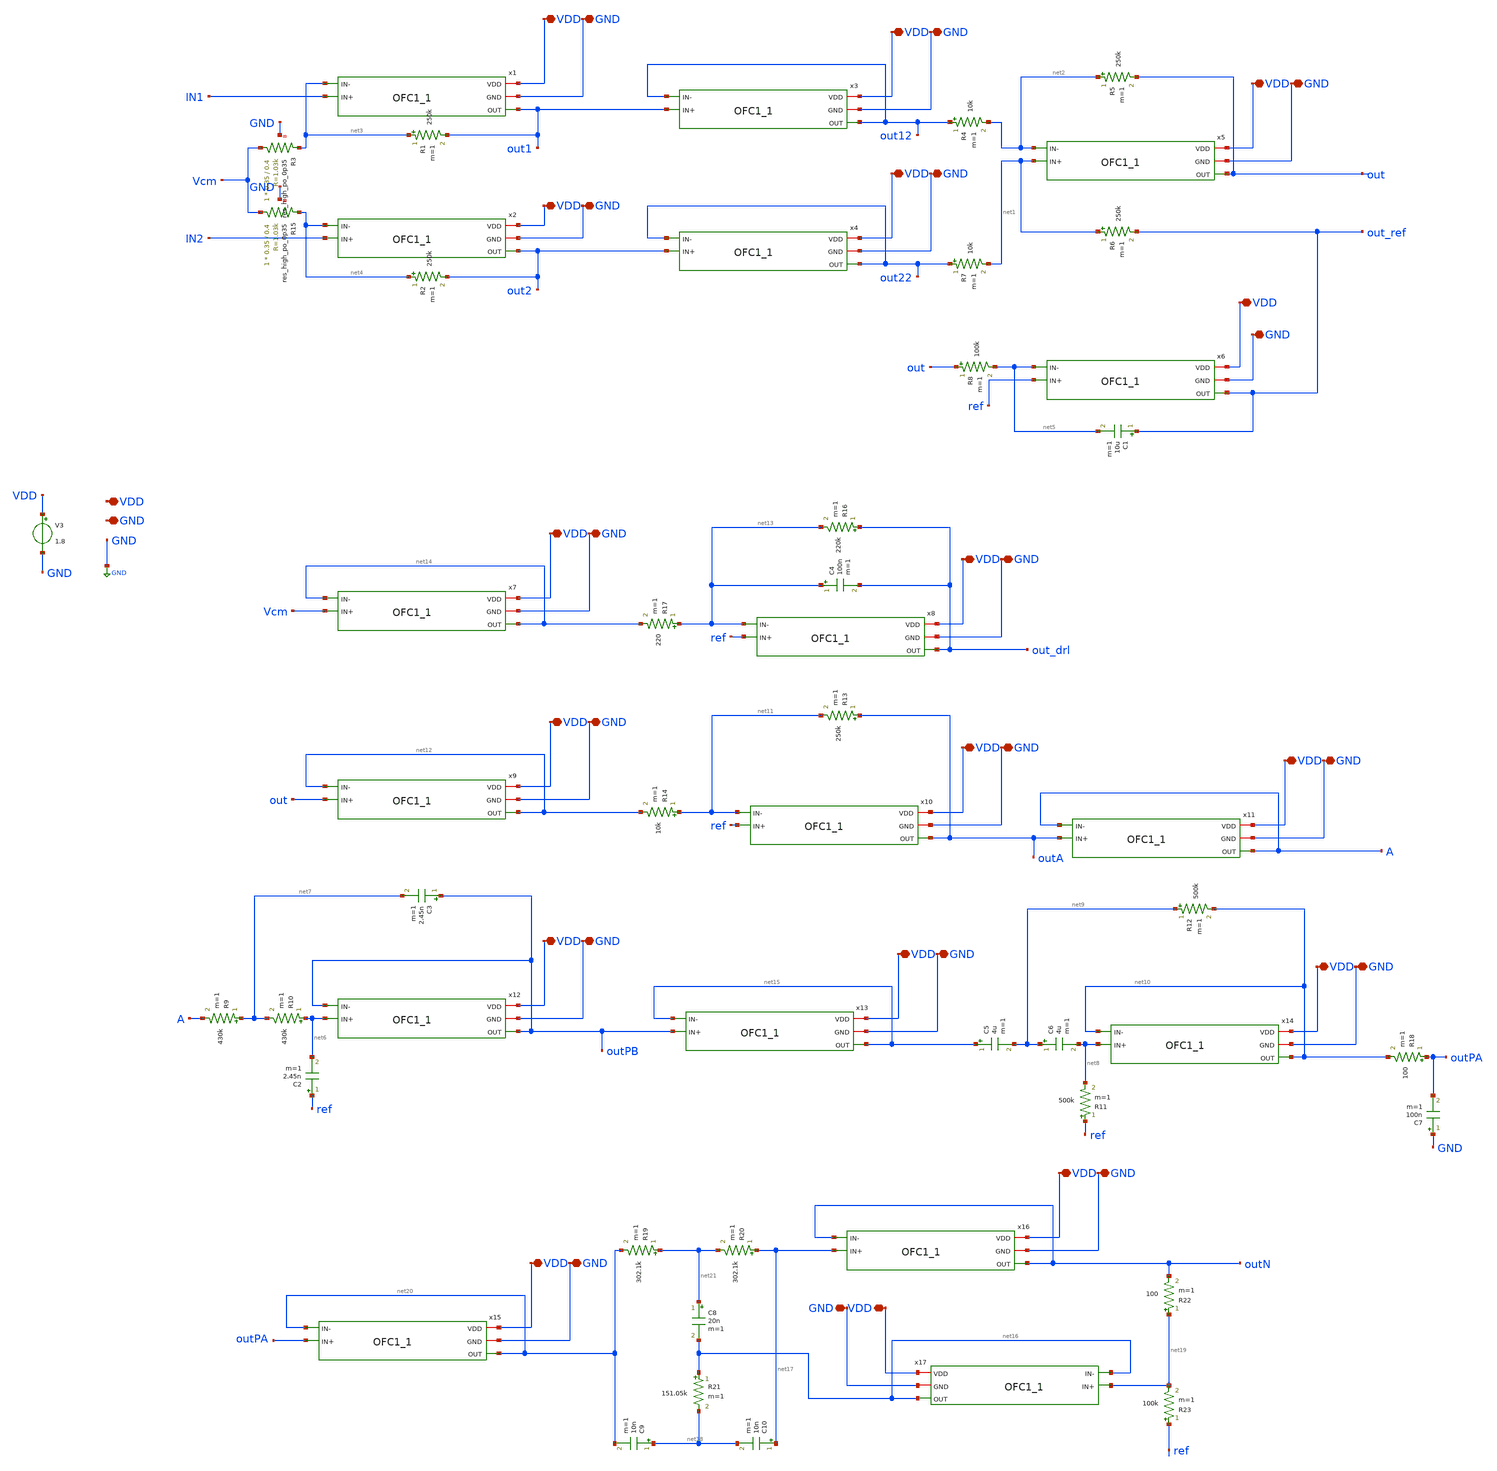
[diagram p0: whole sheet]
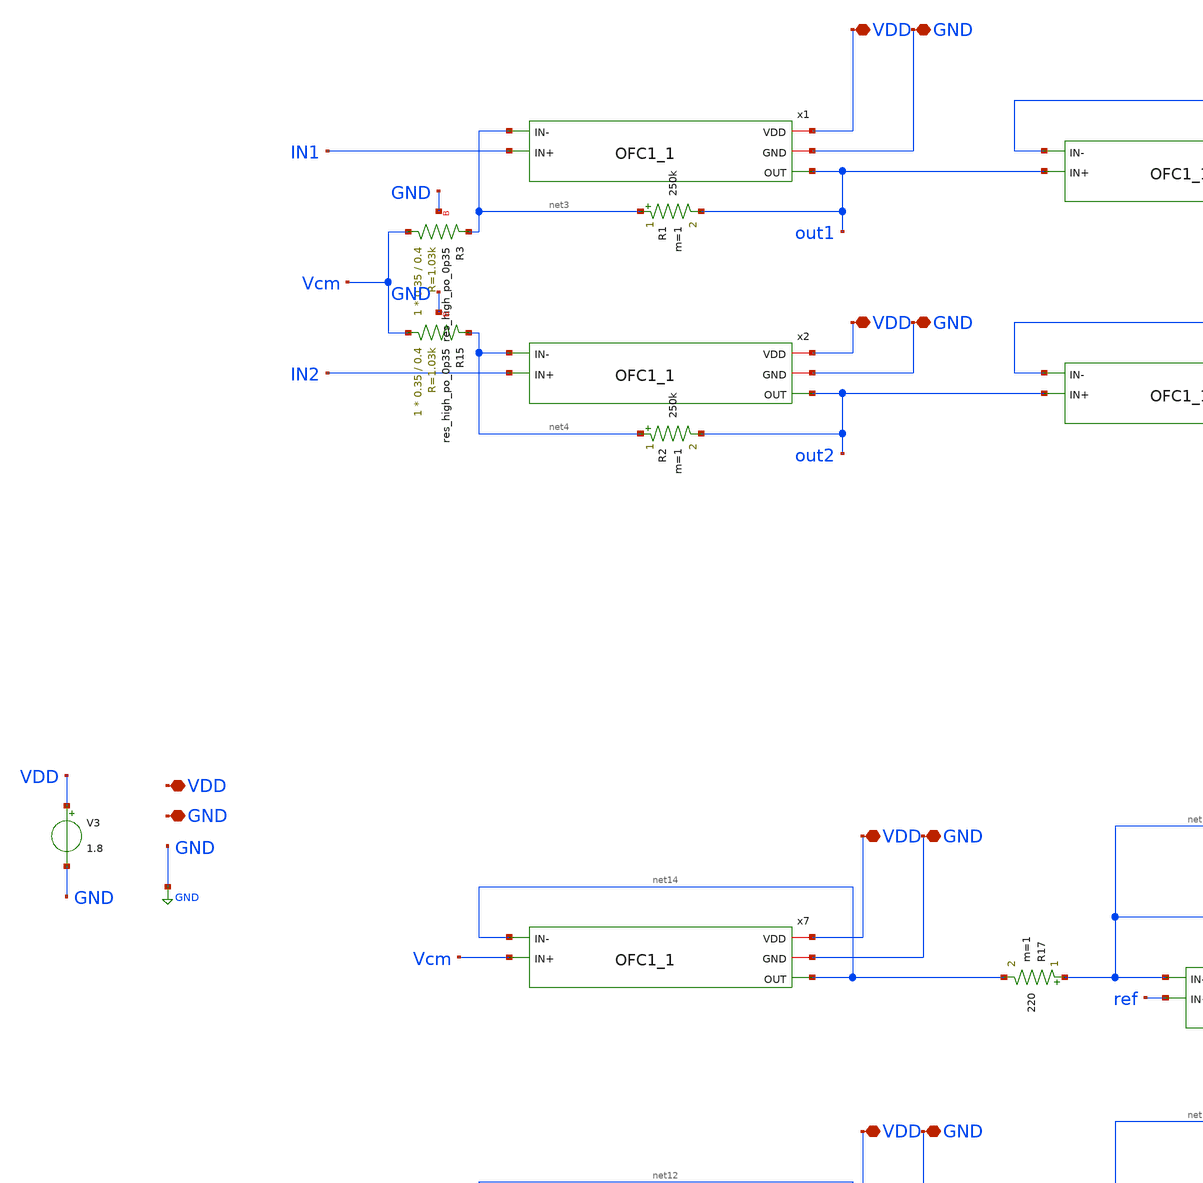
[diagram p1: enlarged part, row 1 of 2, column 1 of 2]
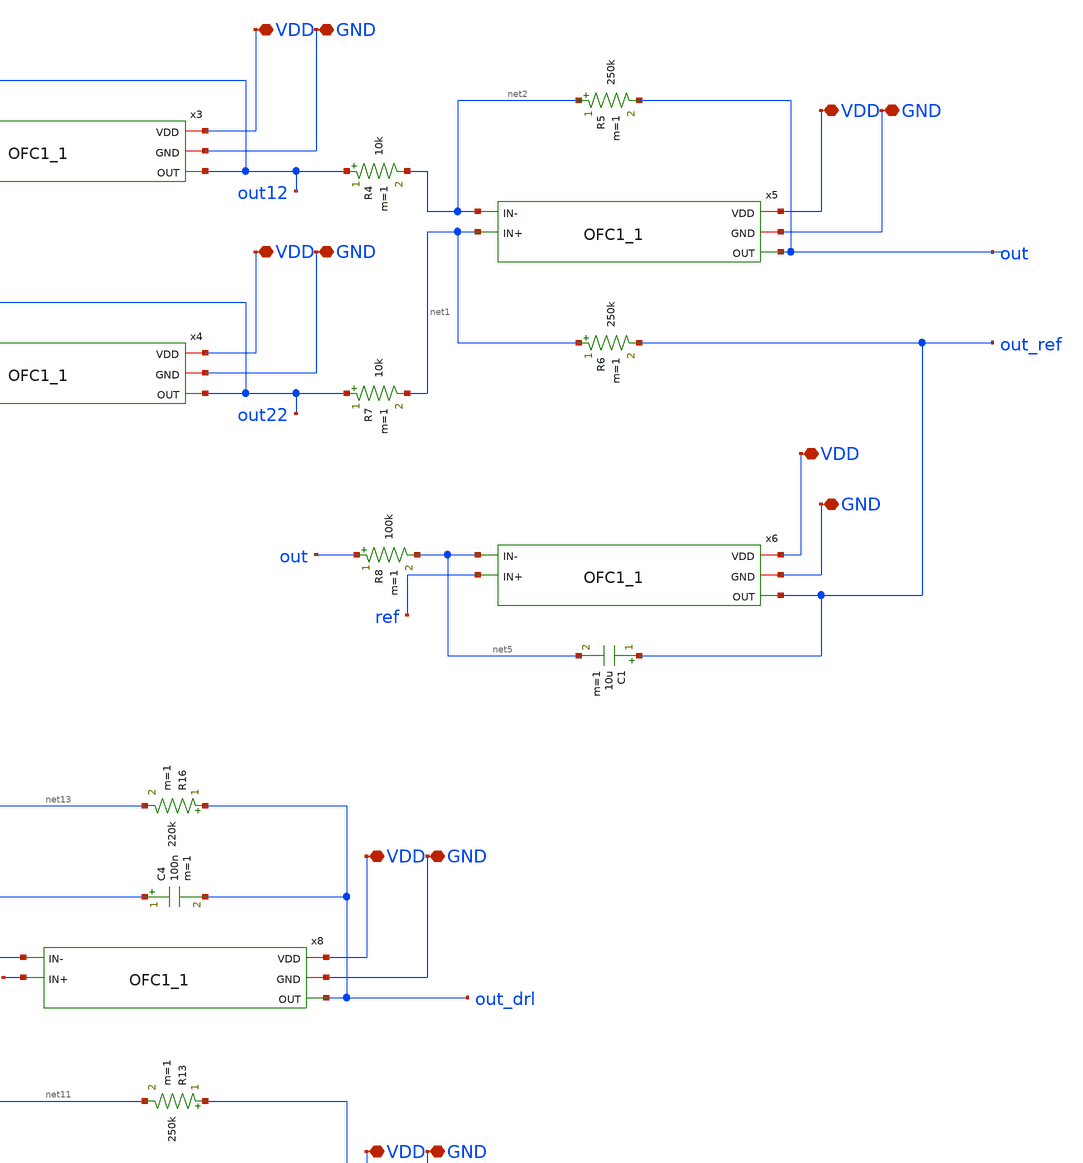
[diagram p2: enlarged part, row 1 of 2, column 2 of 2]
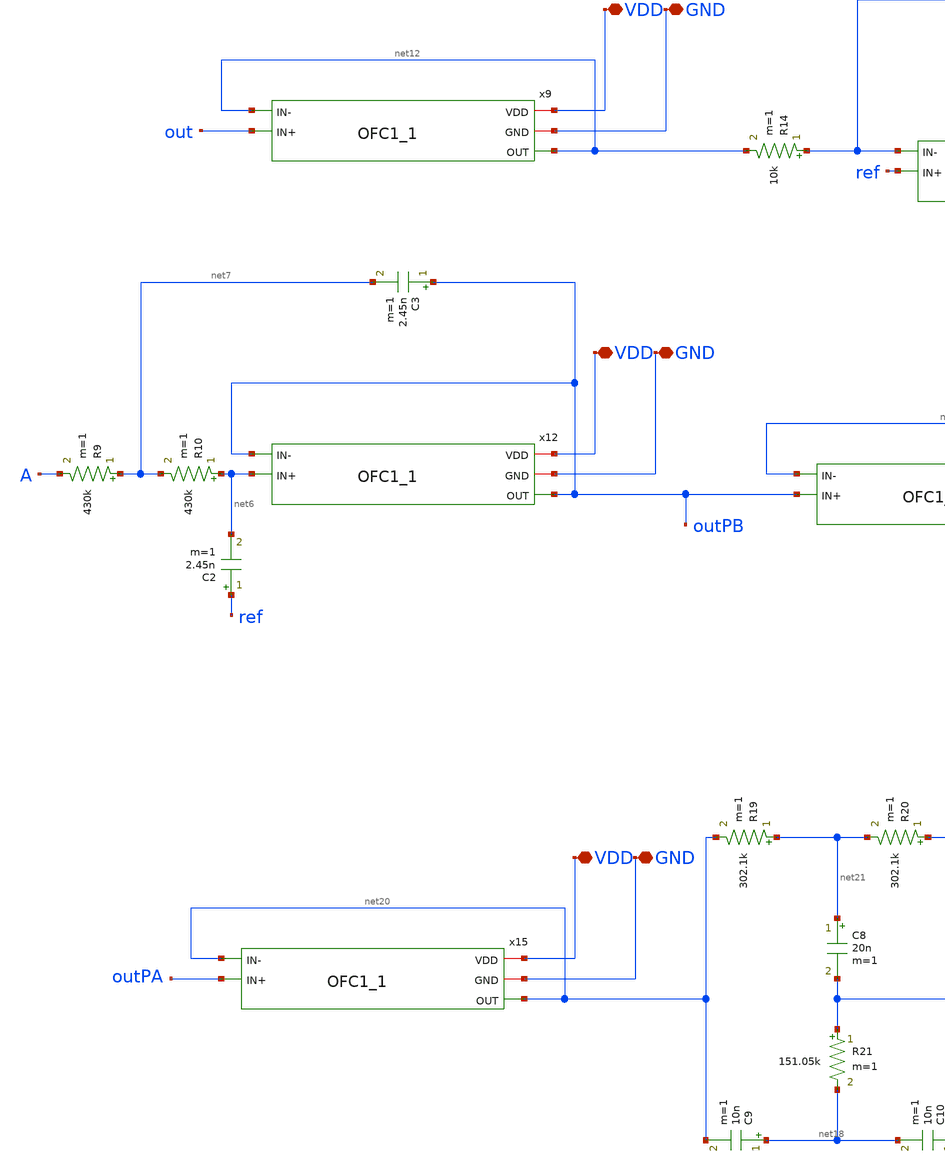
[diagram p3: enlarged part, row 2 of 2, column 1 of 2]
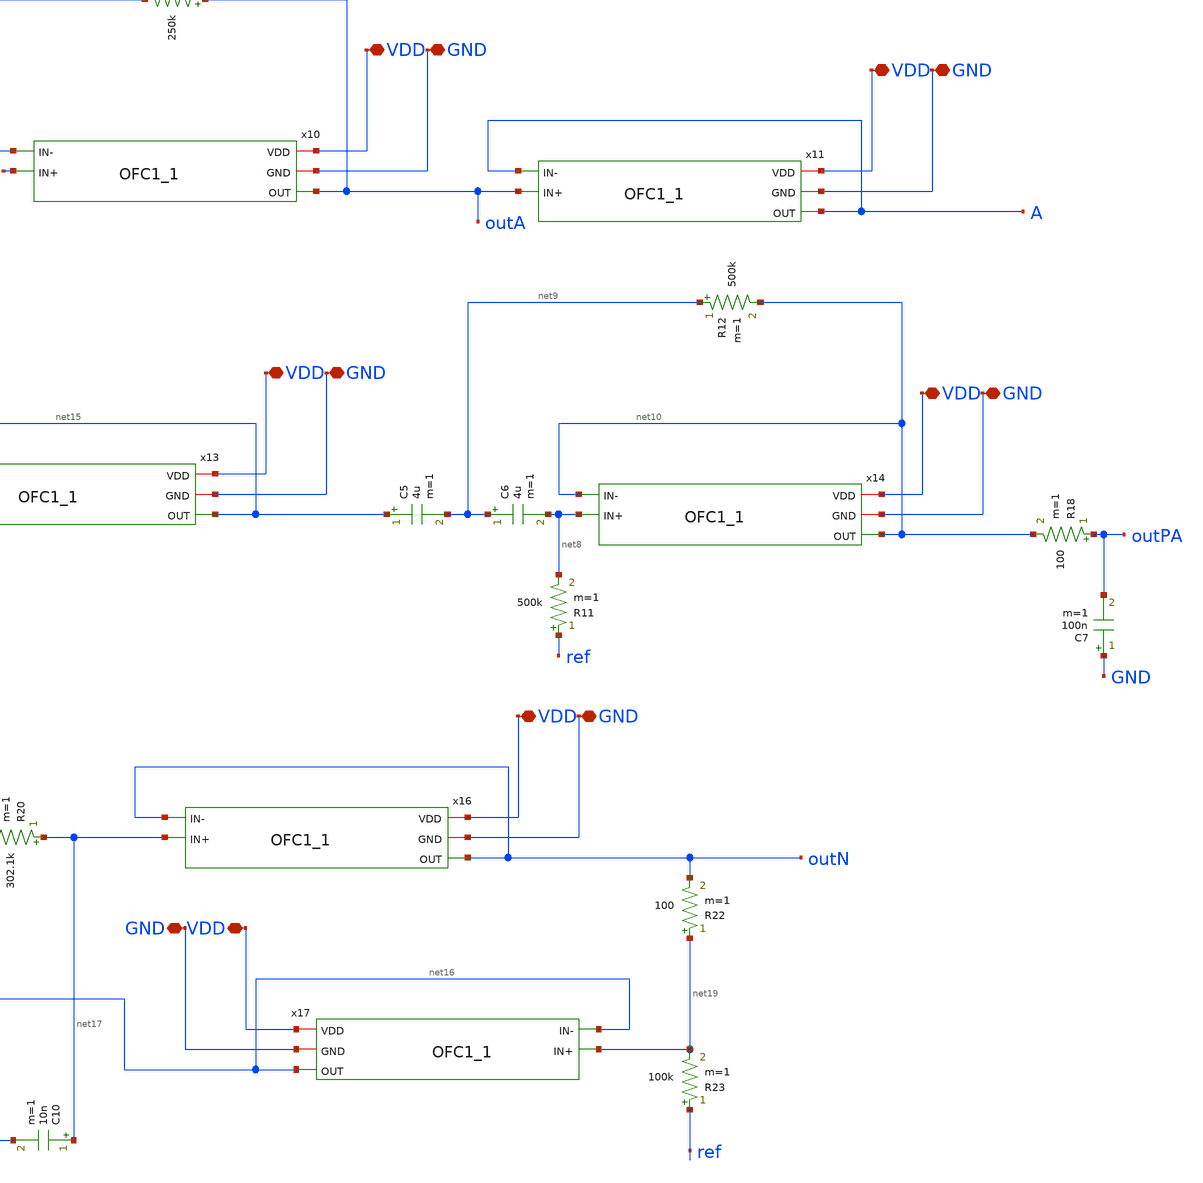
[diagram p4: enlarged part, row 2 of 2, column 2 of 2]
** sch_path: xschem/ecg_pwl1_1.sch
**.subckt ecg_pwl1_1 VDD GND VDD VDD GND GND VDD GND VDD GND VDD GND VDD GND VDD GND VDD GND VDD GND
*+ VDD GND VDD GND VDD GND VDD GND VDD GND VDD GND VDD GND VDD GND
*.iopin VDD
*.iopin GND
*.iopin VDD
*.iopin VDD
*.iopin GND
*.iopin GND
*.iopin VDD
*.iopin GND
*.iopin VDD
*.iopin GND
*.iopin VDD
*.iopin GND
*.iopin VDD
*.iopin GND
*.iopin VDD
*.iopin GND
*.iopin VDD
*.iopin GND
*.iopin VDD
*.iopin GND
*.iopin VDD
*.iopin GND
*.iopin VDD
*.iopin GND
*.iopin VDD
*.iopin GND
*.iopin VDD
*.iopin GND
*.iopin VDD
*.iopin GND
*.iopin VDD
*.iopin GND
*.iopin VDD
*.iopin GND
*.iopin VDD
*.iopin GND
V3 VDD GND 1.8
R1 net3 out1 250k m=1
R2 net4 out2 250k m=1
R6 net1 out_ref 250k m=1
R8 out net5 100k m=1
C1 out_ref net5 10u m=1
R5 net2 out 250k m=1
R4 out12 net2 10k m=1
R7 out22 net1 10k m=1
R9 net7 A 430k m=1
C2 ref net6 2.45n m=1
R10 net6 net7 430k m=1
C3 outPB net7 2.45n m=1
R11 ref net8 500k m=1
C5 net15 net9 4u m=1
C6 net9 net8 4u m=1
R13 outA net11 250k m=1
R14 net11 net12 10k m=1
R16 out_drl net13 220k m=1
R17 net13 net14 220 m=1
C4 net13 out_drl 100n m=1
C7 GND outPA 100n m=1
R18 outPA net10 100 m=1
R12 net9 net10 500k m=1
XR3 Vcm net3 GND sky130_fd_pr__res_high_po_0p35 L=0.4 mult=1 m=1
XR15 Vcm net4 GND sky130_fd_pr__res_high_po_0p35 L=0.4 mult=1 m=1
R19 net21 net20 302.1k m=1
R20 net17 net21 302.1k m=1
R21 net16 net18 151.05k m=1
C8 net21 net16 20n m=1
C9 net18 net20 10n m=1
C10 net17 net18 10n m=1
R22 net19 outN 100 m=1
R23 ref net19 100k m=1
x1 VDD GND out1 net3 IN1 OFC1_1
x2 VDD GND out2 net4 IN2 OFC1_1
x3 VDD GND out12 out12 out1 OFC1_1
x4 VDD GND out22 out22 out2 OFC1_1
x5 VDD GND out net2 net1 OFC1_1
x6 VDD GND out_ref net5 ref OFC1_1
x7 VDD GND net14 net14 Vcm OFC1_1
x8 VDD GND out_drl net13 ref OFC1_1
x9 VDD GND net12 net12 out OFC1_1
x10 VDD GND outA net11 ref OFC1_1
x11 VDD GND A A outA OFC1_1
x12 VDD GND outPB outPB net6 OFC1_1
x13 VDD GND net15 net15 outPB OFC1_1
x14 VDD GND net10 net10 net8 OFC1_1
x15 VDD GND net20 net20 outPA OFC1_1
x16 VDD GND outN outN net17 OFC1_1
x17 VDD GND net16 net16 net19 OFC1_1
**** begin user architecture code


** --- IMPOSTAZIONI DI SIMULAZIONE ---
.option reltol=1e-3 abstol=1e-12 method=gear

* --- DEFINIZIONE GENERATORI (Seguendo Immagine 2026-01-03 122450.png) ---

* V2: Generatore di Bias Principale (Offset 0.9V)
V2 v_offset GND 0.9

* VbiasR3: Generatore di MODO COMUNE (50Hz)
* Iniettato nel punto comune 'ref', sollevato dall'offset di 0.9V
VbiasR3 ref v_offset dc 0 sin(0 100m 50 0 0 0)

* VbiasR1: Braccio Positivo (ECG / 2)
* Collegato tra IN1 e ref. Fase 0.
VbiasR1 IN1 ref dc 0 pwl(   0.00 0.00000 0.05 0.00000 0.08 0.00000 0.10 0.00005 0.12 0.000075   0.15 0.00010 0.18 0.000075 0.22 0.00000 0.28 0.00000 0.29 -0.000025   0.30 -0.00005 0.31 0.00035 0.32 0.00075 0.33 0.00035 0.34 -0.00010   0.35 -0.00005 0.36 0.00000 0.40 0.00000 0.48 0.00000 0.52 0.00005   0.56 0.000125 0.60 0.00015 0.64 0.000125 0.68 0.00005 0.75 0.00000   1.00 0.00000 )

* VbiasR2: Braccio Negativo (ECG / 2 Invertito)
* Collegato tra IN2 e ref. I valori del PWL sono moltiplicati per -1.
VbiasR2 IN2 ref dc 0 pwl(   0.00 0.00000 0.05 0.00000 0.08 0.00000 0.10 -0.00005 0.12 -0.000075   0.15 -0.00010 0.18 -0.000075 0.22 0.00000 0.28 0.00000 0.29 0.000025   0.30 0.00005 0.31 -0.00035 0.32 -0.00075 0.33 -0.00035 0.34 0.00010   0.35 0.00005 0.36 0.00000 0.40 0.00000 0.48 0.00000 0.52 -0.00005   0.56 -0.000125 0.60 -0.00015 0.64 -0.000125 0.68 -0.00005 0.75 0.00000   1.00 0.00000 )

* --- CONTROLLO SIMULAZIONE ---
.control
    * Salvataggio segnali per analisi MATLAB
    save v(IN1) v(IN2) v(ref) v(outN)

    tran 10u 1.1s 0 1m

    * Plot per verifica differenziale
    * L'ECG utile è v(IN1)-v(IN2). Il rumore comune è v(ref)-0.9.
    plot v(IN1) v(IN2) title 'Ingressi OTA: IN1 e IN2 (Differenziali + Comune)'
    plot (v(IN1)-v(IN2)) title 'Segnale ECG Differenziale Puro'
    plot v(outN)
    * Esportazione dati (Tempo, IN1, IN2, Uscita)
    wrdata dati_ecg1.txt  v(outN)
.endc
.end



.lib $::SKYWATER_MODELS/sky130.lib.spice tt
**** end user architecture code
**.ends

* expanding   symbol:  OFC1_1.sym # of pins=5
** sym_path: xschem/OFC1_1.sym
** sch_path: xschem/OFC1_1.sch
.subckt OFC1_1 VDD GND OUT IN- IN+
*.iopin VDD
*.iopin GND
*.ipin IN+
*.ipin IN-
*.opin OUT
XR2 Vb VDD GND sky130_fd_pr__res_xhigh_po_0p35 L=5 mult=1 m=1
XR3 GND Vb GND sky130_fd_pr__res_xhigh_po_0p35 L=13.2 mult=1 m=1
XR1 Vc VDD GND sky130_fd_pr__res_xhigh_po_0p35 L=5 mult=1 m=1
XR4 GND Vc GND sky130_fd_pr__res_xhigh_po_0p35 L=3.07 mult=1 m=1
XR5 Vc1 VDD GND sky130_fd_pr__res_xhigh_po_0p35 L=5 mult=1 m=1
XR6 GND Vc1 GND sky130_fd_pr__res_xhigh_po_0p35 L=13.2 mult=1 m=1
XR7 Vc2 VDD GND sky130_fd_pr__res_xhigh_po_0p35 L=5 mult=1 m=1
XR8 GND Vc2 GND sky130_fd_pr__res_xhigh_po_0p35 L=1.4 mult=1 m=1
XM11 S Vb VDD VDD sky130_fd_pr__pfet_01v8_lvt L=1 W=45 nf=3 ad='int((nf+1)/2) * W/nf * 0.29' as='int((nf+2)/2) * W/nf * 0.29'
+ pd='2*int((nf+1)/2) * (W/nf + 0.29)' ps='2*int((nf+2)/2) * (W/nf + 0.29)' nrd='0.29 / W' nrs='0.29 / W'
+ sa=0 sb=0 sd=0 mult=10 m=10
XM1 D1 IN+ S S sky130_fd_pr__pfet_01v8_lvt L=10 W=50 nf=2 ad='int((nf+1)/2) * W/nf * 0.29' as='int((nf+2)/2) * W/nf * 0.29'
+ pd='2*int((nf+1)/2) * (W/nf + 0.29)' ps='2*int((nf+2)/2) * (W/nf + 0.29)' nrd='0.29 / W' nrs='0.29 / W'
+ sa=0 sb=0 sd=0 mult=2 m=2
XM2 D2 IN- S S sky130_fd_pr__pfet_01v8_lvt L=10 W=50 nf=2 ad='int((nf+1)/2) * W/nf * 0.29' as='int((nf+2)/2) * W/nf * 0.29'
+ pd='2*int((nf+1)/2) * (W/nf + 0.29)' ps='2*int((nf+2)/2) * (W/nf + 0.29)' nrd='0.29 / W' nrs='0.29 / W'
+ sa=0 sb=0 sd=0 mult=2 m=2
XM3 OUT Vc1 D2 GND sky130_fd_pr__nfet_01v8_lvt L=1 W=4 nf=1 ad='int((nf+1)/2) * W/nf * 0.29' as='int((nf+2)/2) * W/nf * 0.29'
+ pd='2*int((nf+1)/2) * (W/nf + 0.29)' ps='2*int((nf+2)/2) * (W/nf + 0.29)' nrd='0.29 / W' nrs='0.29 / W'
+ sa=0 sb=0 sd=0 mult=1 m=1
XM4 D2 Vc GND GND sky130_fd_pr__nfet_01v8_lvt L=1 W=8 nf=1 ad='int((nf+1)/2) * W/nf * 0.29' as='int((nf+2)/2) * W/nf * 0.29'
+ pd='2*int((nf+1)/2) * (W/nf + 0.29)' ps='2*int((nf+2)/2) * (W/nf + 0.29)' nrd='0.29 / W' nrs='0.29 / W'
+ sa=0 sb=0 sd=0 mult=1 m=1
XM5 D1 Vc GND GND sky130_fd_pr__nfet_01v8_lvt L=1 W=8 nf=1 ad='int((nf+1)/2) * W/nf * 0.29' as='int((nf+2)/2) * W/nf * 0.29'
+ pd='2*int((nf+1)/2) * (W/nf + 0.29)' ps='2*int((nf+2)/2) * (W/nf + 0.29)' nrd='0.29 / W' nrs='0.29 / W'
+ sa=0 sb=0 sd=0 mult=1 m=1
XM6 G Vc1 D1 GND sky130_fd_pr__nfet_01v8_lvt L=1 W=4 nf=1 ad='int((nf+1)/2) * W/nf * 0.29' as='int((nf+2)/2) * W/nf * 0.29'
+ pd='2*int((nf+1)/2) * (W/nf + 0.29)' ps='2*int((nf+2)/2) * (W/nf + 0.29)' nrd='0.29 / W' nrs='0.29 / W'
+ sa=0 sb=0 sd=0 mult=1 m=1
XM7 G Vc2 D9 VDD sky130_fd_pr__pfet_01v8_lvt L=1.2 W=8 nf=1 ad='int((nf+1)/2) * W/nf * 0.29' as='int((nf+2)/2) * W/nf * 0.29'
+ pd='2*int((nf+1)/2) * (W/nf + 0.29)' ps='2*int((nf+2)/2) * (W/nf + 0.29)' nrd='0.29 / W' nrs='0.29 / W'
+ sa=0 sb=0 sd=0 mult=1 m=1
XM9 D9 G VDD VDD sky130_fd_pr__pfet_01v8_lvt L=1.2 W=5.7 nf=1 ad='int((nf+1)/2) * W/nf * 0.29' as='int((nf+2)/2) * W/nf * 0.29'
+ pd='2*int((nf+1)/2) * (W/nf + 0.29)' ps='2*int((nf+2)/2) * (W/nf + 0.29)' nrd='0.29 / W' nrs='0.29 / W'
+ sa=0 sb=0 sd=0 mult=1 m=1
XM8 D10 G VDD VDD sky130_fd_pr__pfet_01v8_lvt L=1.2 W=5.7 nf=1 ad='int((nf+1)/2) * W/nf * 0.29' as='int((nf+2)/2) * W/nf * 0.29'
+ pd='2*int((nf+1)/2) * (W/nf + 0.29)' ps='2*int((nf+2)/2) * (W/nf + 0.29)' nrd='0.29 / W' nrs='0.29 / W'
+ sa=0 sb=0 sd=0 mult=1 m=1
XM10 OUT Vc2 D10 VDD sky130_fd_pr__pfet_01v8_lvt L=1.2 W=8 nf=1 ad='int((nf+1)/2) * W/nf * 0.29' as='int((nf+2)/2) * W/nf * 0.29'
+ pd='2*int((nf+1)/2) * (W/nf + 0.29)' ps='2*int((nf+2)/2) * (W/nf + 0.29)' nrd='0.29 / W' nrs='0.29 / W'
+ sa=0 sb=0 sd=0 mult=1 m=1
.ends

.GLOBAL GND
.end
